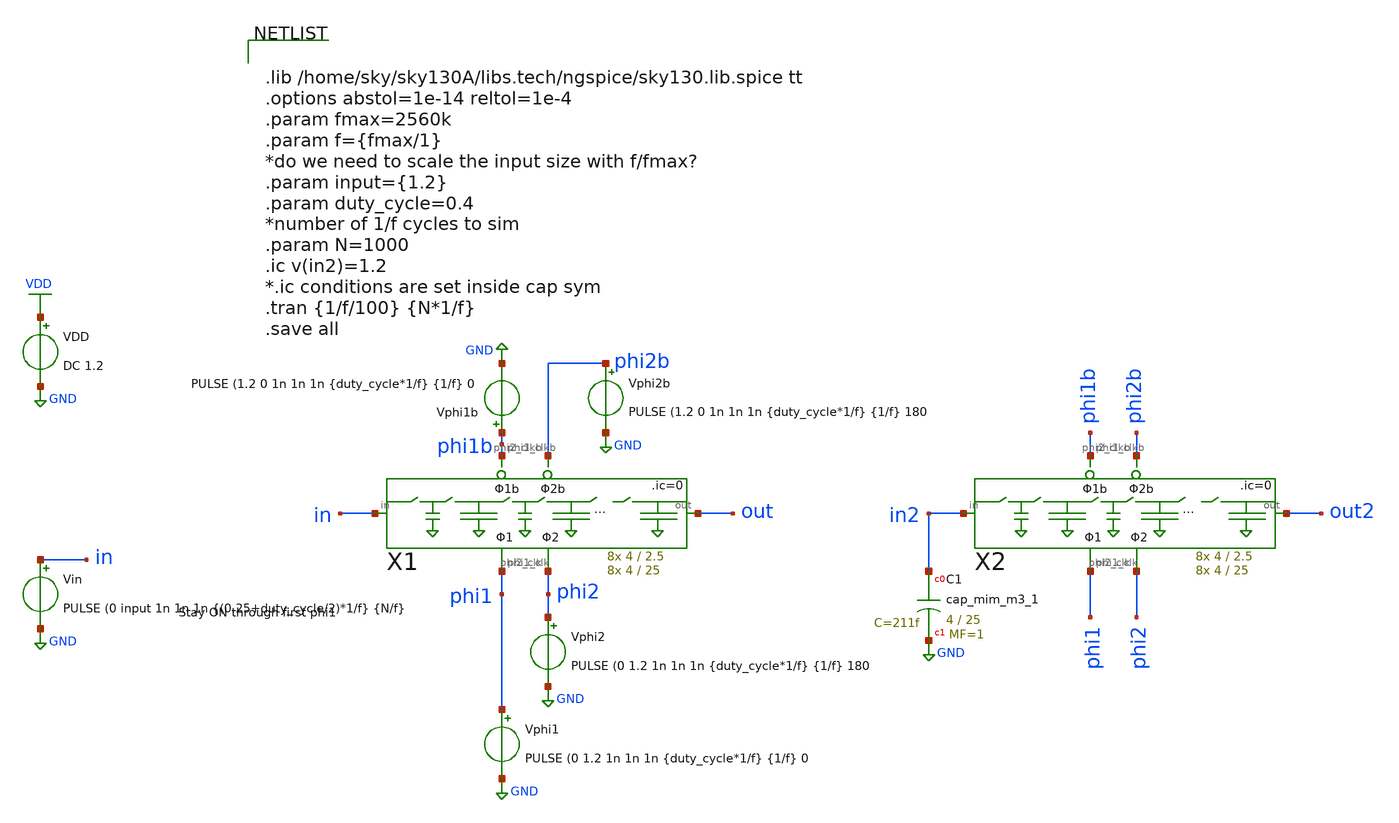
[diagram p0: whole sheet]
** sch_path: xschem/Switched_Caps/16switchcaps_2phi_tb.sch
**.subckt 16switchcaps_2phi_tb
Vin in GND PULSE (0 input 1n 1n 1n {(0.25+duty_cycle/2)*1/f} {N/f}
VDD VDD GND DC 1.2
Vphi1 phi1 GND PULSE (0 1.2 1n 1n 1n {duty_cycle*1/f} {1/f} 0
Vphi1b phi1b GND PULSE (1.2 0 1n 1n 1n {duty_cycle*1/f} {1/f} 0
Vphi2 phi2 GND PULSE (0 1.2 1n 1n 1n {duty_cycle*1/f} {1/f} 180
Vphi2b phi2b GND PULSE (1.2 0 1n 1n 1n {duty_cycle*1/f} {1/f} 180
X1 in out phi1 phi1b phi2 phi2b 16switchcaps_2phi Wcap1=4 Lcap1=2.5 Wcap2=4 Lcap2=25
X2 in2 out2 phi1 phi1b phi2 phi2b 16switchcaps_2phi Wcap1=4 Lcap1=2.5 Wcap2=4 Lcap2=25
XC1 in2 GND sky130_fd_pr__cap_mim_m3_1 W=4 L=25 MF=1 m=1
**** begin user architecture code


.lib /home/sky/sky130A/libs.tech/ngspice/sky130.lib.spice tt
.options abstol=1e-14 reltol=1e-4
.param fmax=2560k
.param f={fmax/1}
*do we need to scale the input size with f/fmax?
.param input={1.2}
.param duty_cycle=0.4
*number of 1/f cycles to sim
.param N=1000
.ic v(in2)=1.2
*.ic conditions are set inside cap sym
.tran {1/f/100} {N*1/f}
.save all


**** end user architecture code
**.ends

* expanding   symbol:  Switched_Caps/16switchcaps_2phi.sym # of pins=6
** sym_path: xschem/Switched_Caps/16switchcaps_2phi.sym
** sch_path: xschem/Switched_Caps/16switchcaps_2phi.sch
.subckt 16switchcaps_2phi in out phi1_clk phi1_clkb phi2_clk phi2_clkb  Wcap1=4 Lcap1=2.5 Wcap2=4
+ Lcap2=25
*.iopin in
*.iopin out
*.ipin phi2_clkb
*.ipin phi1_clkb
*.ipin phi2_clk
*.ipin phi1_clk
X1 in c2 phi2_clk phi1_clk phi1_clkb phi2_clkb 2switchcaps Wcap1=Wcap1 Lcap1=Lcap1 Wcap2=Wcap2
+ Lcap2=Lcap2
X2 c2 c4 phi2_clk phi1_clk phi1_clkb phi2_clkb 2switchcaps Wcap1=Wcap1 Lcap1=Lcap1 Wcap2=Wcap2
+ Lcap2=Lcap2
X3 c4 c6 phi2_clk phi1_clk phi1_clkb phi2_clkb 2switchcaps Wcap1=Wcap1 Lcap1=Lcap1 Wcap2=Wcap2
+ Lcap2=Lcap2
X4 c6 c8 phi2_clk phi1_clk phi1_clkb phi2_clkb 2switchcaps Wcap1=Wcap1 Lcap1=Lcap1 Wcap2=Wcap2
+ Lcap2=Lcap2
X5 c8 c10 phi2_clk phi1_clk phi1_clkb phi2_clkb 2switchcaps Wcap1=Wcap1 Lcap1=Lcap1 Wcap2=Wcap2
+ Lcap2=Lcap2
X6 c10 c12 phi2_clk phi1_clk phi1_clkb phi2_clkb 2switchcaps Wcap1=Wcap1 Lcap1=Lcap1 Wcap2=Wcap2
+ Lcap2=Lcap2
X7 c12 c14 phi2_clk phi1_clk phi1_clkb phi2_clkb 2switchcaps Wcap1=Wcap1 Lcap1=Lcap1 Wcap2=Wcap2
+ Lcap2=Lcap2
X8 c14 out phi2_clk phi1_clk phi1_clkb phi2_clkb 2switchcaps Wcap1=Wcap1 Lcap1=Lcap1 Wcap2=Wcap2
+ Lcap2=Lcap2
.ends


* expanding   symbol:  Switched_Caps/2switchcaps.sym # of pins=6
** sym_path: xschem/Switched_Caps/2switchcaps.sym
** sch_path: xschem/Switched_Caps/2switchcaps.sch
.subckt 2switchcaps in out phi2_clk_n phi1_clk_n phi1_clk_p phi2_clk_p  Wcap1=4 Lcap1=2.5 Wcap2=4
+ Lcap2=25
*.iopin out
*.iopin in
*.ipin phi1_clk_n
*.ipin phi1_clk_p
*.ipin phi2_clk_p
*.ipin phi2_clk_n
XC1 c1 GND sky130_fd_pr__cap_mim_m3_1 W=Wcap1 L=Lcap1 MF=1 m=1
XC2 out GND sky130_fd_pr__cap_mim_m3_1 W=Wcap2 L=Lcap2 MF=1 m=1
**** begin user architecture code

.ic v(c1)=0 v(out)=0

**** end user architecture code
X1 in c1 phi1_clk_p phi1_clk_n transmission_gate Wpmos=0.42 Lpmos=0.18 Wnmos=0.42 Lnmos=0.18
X2 c1 out phi2_clk_p phi2_clk_n transmission_gate Wpmos=0.42 Lpmos=0.18 Wnmos=0.42 Lnmos=0.18
.ends


* expanding   symbol:  transmission_gate/transmission_gate.sym # of pins=4
** sym_path: xschem/transmission_gate/transmission_gate.sym
** sch_path: xschem/transmission_gate/transmission_gate.sch
.subckt transmission_gate in out ctrl_ ctrl  Wpmos=0.42 Lpmos=0.18 Wnmos=0.42 Lnmos=0.18
*.iopin in
*.iopin out
*.ipin ctrl_
*.ipin ctrl
XM1 out ctrl in GND sky130_fd_pr__nfet_01v8 L=Lnmos W=Wnmos nf=1 ad='int((nf+1)/2) * W/nf * 0.29' as='int((nf+2)/2) * W/nf * 0.29'
+ pd='2*int((nf+1)/2) * (W/nf + 0.29)' ps='2*int((nf+2)/2) * (W/nf + 0.29)' nrd='0.29 / W' nrs='0.29 / W'
+ sa=0 sb=0 sd=0 mult=1 m=1
XM2 out ctrl_ in VDD sky130_fd_pr__pfet_01v8 L=Lpmos W=Wpmos nf=1 ad='int((nf+1)/2) * W/nf * 0.29' as='int((nf+2)/2) * W/nf * 0.29'
+ pd='2*int((nf+1)/2) * (W/nf + 0.29)' ps='2*int((nf+2)/2) * (W/nf + 0.29)' nrd='0.29 / W' nrs='0.29 / W'
+ sa=0 sb=0 sd=0 mult=1 m=1
.ends

.GLOBAL GND
.GLOBAL VDD
.end
